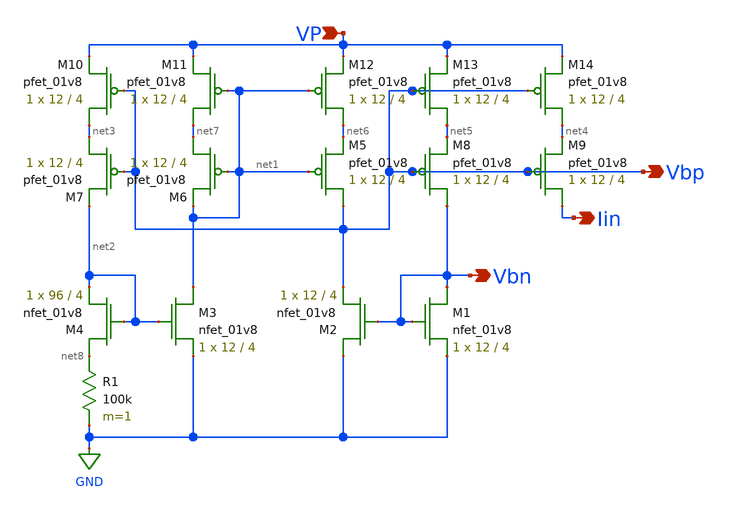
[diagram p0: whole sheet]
** sch_path: xschem/biasGen.sch
**.subckt biasGen Iin Vbp Vbn VP
*.opin Iin
*.opin Vbp
*.opin Vbn
*.ipin VP
XM1 Vbn Vbn GND GND sky130_fd_pr__nfet_01v8 L=4 W=12 nf=1 ad='int((nf+1)/2) * W/nf * 0.29' as='int((nf+2)/2) * W/nf * 0.29'
+ pd='2*int((nf+1)/2) * (W/nf + 0.29)' ps='2*int((nf+2)/2) * (W/nf + 0.29)' nrd='0.29 / W' nrs='0.29 / W'
+ sa=0 sb=0 sd=0 mult=1 m=1
XM2 GND Vbn Vbp GND sky130_fd_pr__nfet_01v8 L=4 W=12 nf=1 ad='int((nf+1)/2) * W/nf * 0.29' as='int((nf+2)/2) * W/nf * 0.29'
+ pd='2*int((nf+1)/2) * (W/nf + 0.29)' ps='2*int((nf+2)/2) * (W/nf + 0.29)' nrd='0.29 / W' nrs='0.29 / W'
+ sa=0 sb=0 sd=0 mult=1 m=1
XM3 net1 net2 GND GND sky130_fd_pr__nfet_01v8 L=4 W=12 nf=1 ad='int((nf+1)/2) * W/nf * 0.29' as='int((nf+2)/2) * W/nf * 0.29'
+ pd='2*int((nf+1)/2) * (W/nf + 0.29)' ps='2*int((nf+2)/2) * (W/nf + 0.29)' nrd='0.29 / W' nrs='0.29 / W'
+ sa=0 sb=0 sd=0 mult=1 m=1
XM4 net8 net2 net2 GND sky130_fd_pr__nfet_01v8 L=4 W=96 nf=1 ad='int((nf+1)/2) * W/nf * 0.29' as='int((nf+2)/2) * W/nf * 0.29'
+ pd='2*int((nf+1)/2) * (W/nf + 0.29)' ps='2*int((nf+2)/2) * (W/nf + 0.29)' nrd='0.29 / W' nrs='0.29 / W'
+ sa=0 sb=0 sd=0 mult=1 m=1
XM5 Vbp net1 net6 VDD sky130_fd_pr__pfet_01v8 L=4 W=12 nf=1 ad='int((nf+1)/2) * W/nf * 0.29' as='int((nf+2)/2) * W/nf * 0.29'
+ pd='2*int((nf+1)/2) * (W/nf + 0.29)' ps='2*int((nf+2)/2) * (W/nf + 0.29)' nrd='0.29 / W' nrs='0.29 / W'
+ sa=0 sb=0 sd=0 mult=1 m=1
XM6 net7 net1 net1 VDD sky130_fd_pr__pfet_01v8 L=4 W=12 nf=1 ad='int((nf+1)/2) * W/nf * 0.29' as='int((nf+2)/2) * W/nf * 0.29'
+ pd='2*int((nf+1)/2) * (W/nf + 0.29)' ps='2*int((nf+2)/2) * (W/nf + 0.29)' nrd='0.29 / W' nrs='0.29 / W'
+ sa=0 sb=0 sd=0 mult=1 m=1
XM7 net3 Vbp net2 VDD sky130_fd_pr__pfet_01v8 L=4 W=12 nf=1 ad='int((nf+1)/2) * W/nf * 0.29' as='int((nf+2)/2) * W/nf * 0.29'
+ pd='2*int((nf+1)/2) * (W/nf + 0.29)' ps='2*int((nf+2)/2) * (W/nf + 0.29)' nrd='0.29 / W' nrs='0.29 / W'
+ sa=0 sb=0 sd=0 mult=1 m=1
XM8 Vbn Vbp net5 VDD sky130_fd_pr__pfet_01v8 L=4 W=12 nf=1 ad='int((nf+1)/2) * W/nf * 0.29' as='int((nf+2)/2) * W/nf * 0.29'
+ pd='2*int((nf+1)/2) * (W/nf + 0.29)' ps='2*int((nf+2)/2) * (W/nf + 0.29)' nrd='0.29 / W' nrs='0.29 / W'
+ sa=0 sb=0 sd=0 mult=1 m=1
R1 net8 GND 100k m=1
XM9 Iin Vbp net4 VDD sky130_fd_pr__pfet_01v8 L=4 W=12 nf=1 ad='int((nf+1)/2) * W/nf * 0.29' as='int((nf+2)/2) * W/nf * 0.29'
+ pd='2*int((nf+1)/2) * (W/nf + 0.29)' ps='2*int((nf+2)/2) * (W/nf + 0.29)' nrd='0.29 / W' nrs='0.29 / W'
+ sa=0 sb=0 sd=0 mult=1 m=1
XM10 net3 Vbp VP VDD sky130_fd_pr__pfet_01v8 L=4 W=12 nf=1 ad='int((nf+1)/2) * W/nf * 0.29' as='int((nf+2)/2) * W/nf * 0.29'
+ pd='2*int((nf+1)/2) * (W/nf + 0.29)' ps='2*int((nf+2)/2) * (W/nf + 0.29)' nrd='0.29 / W' nrs='0.29 / W'
+ sa=0 sb=0 sd=0 mult=1 m=1
XM11 net7 net1 VP VDD sky130_fd_pr__pfet_01v8 L=4 W=12 nf=1 ad='int((nf+1)/2) * W/nf * 0.29' as='int((nf+2)/2) * W/nf * 0.29'
+ pd='2*int((nf+1)/2) * (W/nf + 0.29)' ps='2*int((nf+2)/2) * (W/nf + 0.29)' nrd='0.29 / W' nrs='0.29 / W'
+ sa=0 sb=0 sd=0 mult=1 m=1
XM12 net6 net1 VP VDD sky130_fd_pr__pfet_01v8 L=4 W=12 nf=1 ad='int((nf+1)/2) * W/nf * 0.29' as='int((nf+2)/2) * W/nf * 0.29'
+ pd='2*int((nf+1)/2) * (W/nf + 0.29)' ps='2*int((nf+2)/2) * (W/nf + 0.29)' nrd='0.29 / W' nrs='0.29 / W'
+ sa=0 sb=0 sd=0 mult=1 m=1
XM13 net5 Vbp VP VDD sky130_fd_pr__pfet_01v8 L=4 W=12 nf=1 ad='int((nf+1)/2) * W/nf * 0.29' as='int((nf+2)/2) * W/nf * 0.29'
+ pd='2*int((nf+1)/2) * (W/nf + 0.29)' ps='2*int((nf+2)/2) * (W/nf + 0.29)' nrd='0.29 / W' nrs='0.29 / W'
+ sa=0 sb=0 sd=0 mult=1 m=1
XM14 net4 Vbp VP VDD sky130_fd_pr__pfet_01v8 L=4 W=12 nf=1 ad='int((nf+1)/2) * W/nf * 0.29' as='int((nf+2)/2) * W/nf * 0.29'
+ pd='2*int((nf+1)/2) * (W/nf + 0.29)' ps='2*int((nf+2)/2) * (W/nf + 0.29)' nrd='0.29 / W' nrs='0.29 / W'
+ sa=0 sb=0 sd=0 mult=1 m=1
**.ends
.GLOBAL GND
.end
